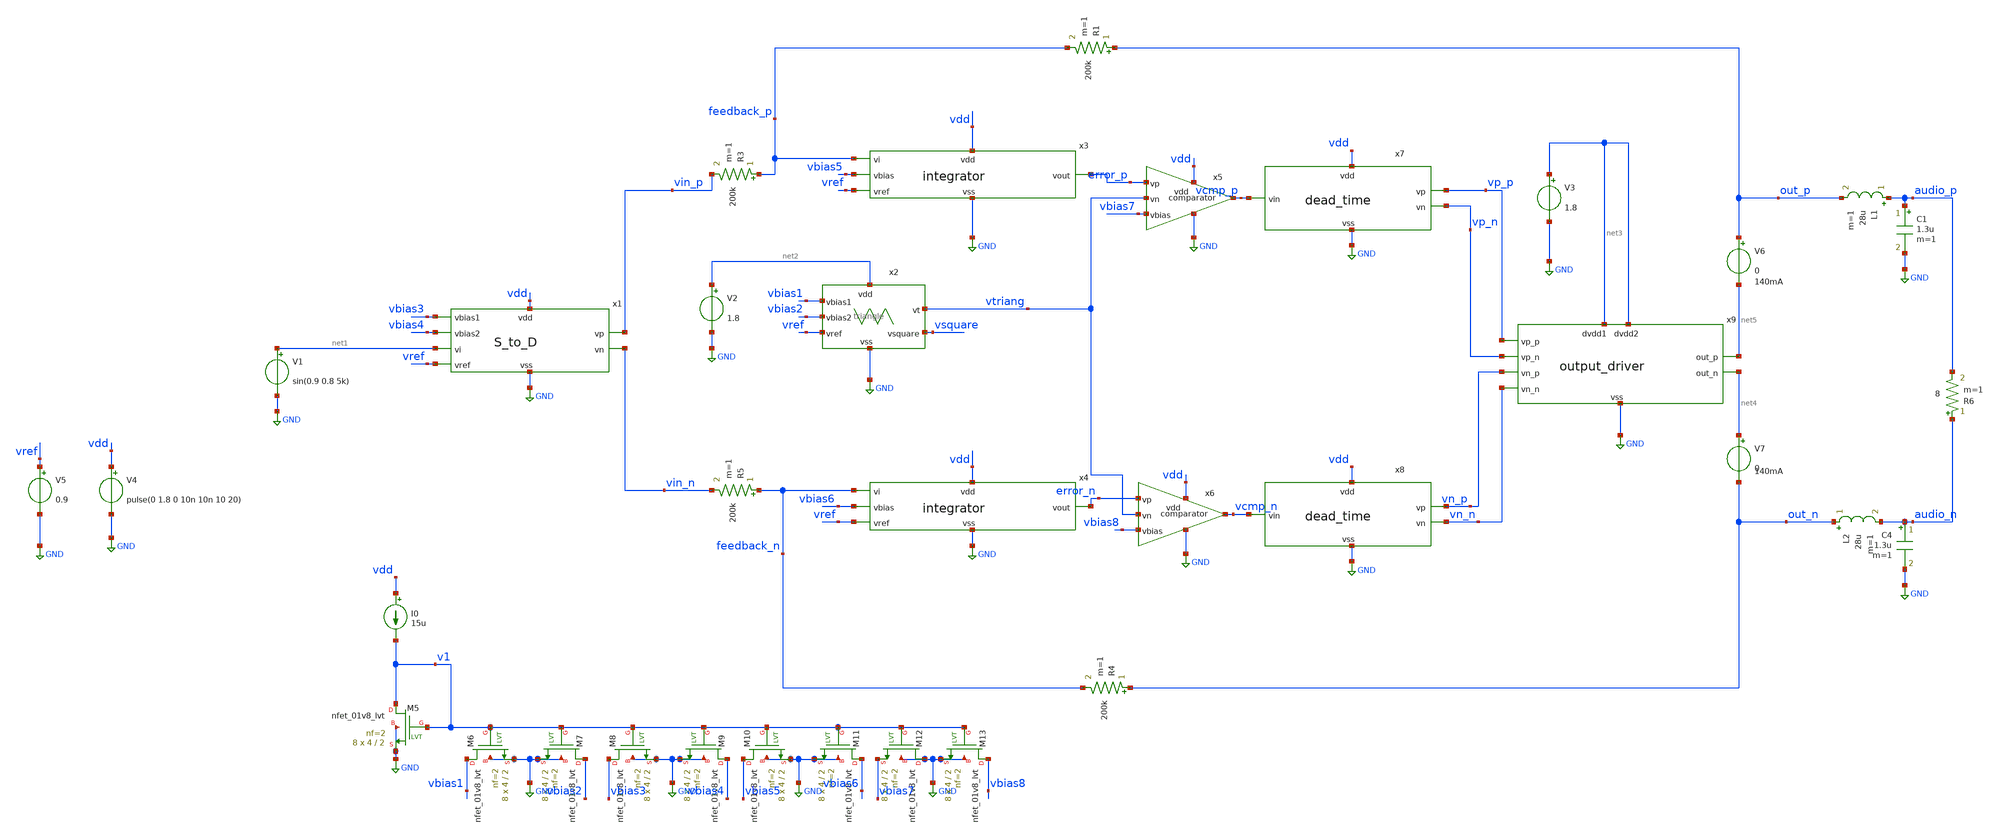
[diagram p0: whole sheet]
** sch_path: xschem/src/Class_D/Class_D_revised_tb.sch
**.subckt Class_D_revised_tb
V1 net1 GND sin(0.9 0.8 5k)
V5 vref GND 0.9
L1 audio_p out_p 28u m=1
C1 audio_p GND 1.3u m=1
R1 out_p feedback_p 200k m=1
R3 feedback_p vin_p 200k m=1
R4 out_n feedback_n 200k m=1
R5 feedback_n vin_n 200k m=1
L2 out_n audio_n 28u m=1
C4 audio_n GND 1.3u m=1
R6 audio_n audio_p 8 m=1
V4 vdd GND pulse(0 1.8 0 10n 10n 10 20)
I0 vdd v1 15u
XM5 v1 v1 GND GND sky130_fd_pr__nfet_01v8_lvt L=2 W=4 nf=2 ad='int((nf+1)/2) * W/nf * 0.29' as='int((nf+2)/2) * W/nf * 0.29'
+ pd='2*int((nf+1)/2) * (W/nf + 0.29)' ps='2*int((nf+2)/2) * (W/nf + 0.29)' nrd='0.29 / W' nrs='0.29 / W'
+ sa=0 sb=0 sd=0 mult=8 m=8
XM6 vbias1 v1 GND GND sky130_fd_pr__nfet_01v8_lvt L=2 W=4 nf=2 ad='int((nf+1)/2) * W/nf * 0.29' as='int((nf+2)/2) * W/nf * 0.29'
+ pd='2*int((nf+1)/2) * (W/nf + 0.29)' ps='2*int((nf+2)/2) * (W/nf + 0.29)' nrd='0.29 / W' nrs='0.29 / W'
+ sa=0 sb=0 sd=0 mult=8 m=8
XM7 vbias2 v1 GND GND sky130_fd_pr__nfet_01v8_lvt L=2 W=4 nf=2 ad='int((nf+1)/2) * W/nf * 0.29' as='int((nf+2)/2) * W/nf * 0.29'
+ pd='2*int((nf+1)/2) * (W/nf + 0.29)' ps='2*int((nf+2)/2) * (W/nf + 0.29)' nrd='0.29 / W' nrs='0.29 / W'
+ sa=0 sb=0 sd=0 mult=8 m=8
XM8 vbias3 v1 GND GND sky130_fd_pr__nfet_01v8_lvt L=2 W=4 nf=2 ad='int((nf+1)/2) * W/nf * 0.29' as='int((nf+2)/2) * W/nf * 0.29'
+ pd='2*int((nf+1)/2) * (W/nf + 0.29)' ps='2*int((nf+2)/2) * (W/nf + 0.29)' nrd='0.29 / W' nrs='0.29 / W'
+ sa=0 sb=0 sd=0 mult=8 m=8
XM9 vbias4 v1 GND GND sky130_fd_pr__nfet_01v8_lvt L=2 W=4 nf=2 ad='int((nf+1)/2) * W/nf * 0.29' as='int((nf+2)/2) * W/nf * 0.29'
+ pd='2*int((nf+1)/2) * (W/nf + 0.29)' ps='2*int((nf+2)/2) * (W/nf + 0.29)' nrd='0.29 / W' nrs='0.29 / W'
+ sa=0 sb=0 sd=0 mult=8 m=8
XM10 vbias5 v1 GND GND sky130_fd_pr__nfet_01v8_lvt L=2 W=4 nf=2 ad='int((nf+1)/2) * W/nf * 0.29' as='int((nf+2)/2) * W/nf * 0.29'
+ pd='2*int((nf+1)/2) * (W/nf + 0.29)' ps='2*int((nf+2)/2) * (W/nf + 0.29)' nrd='0.29 / W' nrs='0.29 / W'
+ sa=0 sb=0 sd=0 mult=8 m=8
XM11 vbias6 v1 GND GND sky130_fd_pr__nfet_01v8_lvt L=2 W=4 nf=2 ad='int((nf+1)/2) * W/nf * 0.29' as='int((nf+2)/2) * W/nf * 0.29'
+ pd='2*int((nf+1)/2) * (W/nf + 0.29)' ps='2*int((nf+2)/2) * (W/nf + 0.29)' nrd='0.29 / W' nrs='0.29 / W'
+ sa=0 sb=0 sd=0 mult=8 m=8
XM12 GND v1 vbias7 GND sky130_fd_pr__nfet_01v8_lvt L=2 W=4 nf=2 ad='int((nf+1)/2) * W/nf * 0.29' as='int((nf+2)/2) * W/nf * 0.29'
+ pd='2*int((nf+1)/2) * (W/nf + 0.29)' ps='2*int((nf+2)/2) * (W/nf + 0.29)' nrd='0.29 / W' nrs='0.29 / W'
+ sa=0 sb=0 sd=0 mult=8 m=8
XM13 vbias8 v1 GND GND sky130_fd_pr__nfet_01v8_lvt L=2 W=4 nf=2 ad='int((nf+1)/2) * W/nf * 0.29' as='int((nf+2)/2) * W/nf * 0.29'
+ pd='2*int((nf+1)/2) * (W/nf + 0.29)' ps='2*int((nf+2)/2) * (W/nf + 0.29)' nrd='0.29 / W' nrs='0.29 / W'
+ sa=0 sb=0 sd=0 mult=8 m=8
V2 net2 GND 1.8
V3 net3 GND 1.8
x1 vdd vbias3 vbias4 net1 vref GND vin_n vin_p S_to_D
x2 net2 vbias1 vbias2 vref GND vsquare vtriang triangle
x3 vdd feedback_p vbias5 vref GND error_p integrator
x4 vdd feedback_n vbias6 vref GND error_n integrator
x5 vdd error_p vtriang vbias7 GND vcmp_p comparator
x6 vdd error_n vtriang vbias8 GND vcmp_n comparator
x7 vdd vcmp_p vp_p vp_n GND dead_time
x8 vdd vcmp_n vn_p vn_n GND dead_time
x9 net3 vp_p net5 GND vp_n net3 vn_p net4 vn_n output_driver
V6 out_p net5 0
V7 net4 out_n 0
**** begin user architecture code


.option rshunt=1e20
.nodeset V(audio_p)=0.9 V(audio_n)=0.9 V(vp_p)=0.79 V(vn_p)=0 V(vcmp_p)=0.859  V(vp_n)=0.79
+ V(vn_n)=0 V(vcmp_n)=0.859 v(vin_p)=0.9 v(vin_n)=0.9 v(vtriang)=0.9
*.nodeset all=0.9
*.option VNTOL=1e-6 ABSTOL=1e-9
*.option savecurrents
*set the absolute voltage error tolerance and absolute current error tolerance
.control
save out_p out_n audio_p audio_n I(V4) I(V2) @r6[i] @r1[i] i(v3) i(v6) vtriang vin_p vin_n error_p
+ error_n vcmp_p vcmp_n vp_p vp_n vn_p vn_n i(v7)
*save vtriang audio_p audio_n I(V2) @r6[i] out_p out_n
*op
tran 3n 10m
*linearize V(audio)
*linearize V(out)
*fft V(out)
*fft V(audio)
*plot mag(V(audio))
*plot mag(V(out))
let pout=@r6[i]*(V(audio_p)-V(audio_n))
let pin=1.8*(I(V4)+I(V2)+I(V3))
meas tran pload avg pout from=2m to=9m
meas tran p_supply avg pin from=2m to=9m
*print pload/p_supply
set nfreqs=20
*fourier 10k V(out_p)-V(out_n)

fourier 5k V(audio_p)-V(audio_n)
write class_d_5k_08_output_current_test.raw

.endc





.include /home/eda/pdk/skywater-pdk/libraries/sky130_fd_pr_ngspice/latest/models/corners/tt.spice
.include /home/eda/magic/class_d_audio_amplifier/OTA/OTA_int_post.spice
.include /home/eda/magic/class_d_audio_amplifier/OTA/OTA_post.spice
.include /home/eda/magic/class_d_audio_amplifier/S_to_D/S_to_D_post.spice
.include /home/eda/magic/class_d_audio_amplifier/triang/triangle_post.spice
.include /home/eda/magic/class_d_audio_amplifier/comparator/comparator_post.spice
.include /home/eda/magic/class_d_audio_amplifier/dead_time/dead_time_post.spice
.include /home/eda/magic/class_d_audio_amplifier/output_driver/output_driver_post.spice
* Resistor$::SKYWATER_MODELS/Capacitor
.include $::SKYWATER_MODELS/models/r+c/res_typical__cap_typical.spice
.include $::SKYWATER_MODELS/models/r+c/res_typical__cap_typical__lin.spice
* Special cells
.include $::SKYWATER_MODELS/models/corners/tt/specialized_cells.spice


**** end user architecture code
**.ends

* expanding   symbol:  src/S_to_D/S_to_D.sym # of pins=8
** sym_path: xschem/src/S_to_D/S_to_D.sym
** sch_path: xschem/src/S_to_D/S_to_D.sch
.subckt S_to_D vdd vbias1 vbias2 vi vref vss vn vp
*.iopin vdd
*.iopin vss
*.ipin vi
*.opin vp
*.opin vn
*.ipin vref
*.ipin vbias1
*.ipin vbias2
x1 vdd vref v1 vbias2 vss vn OTA
XR2 vn v1 vss sky130_fd_pr__res_xhigh_po L=10 mult=1 m=1
x2 vdd vi vp vbias1 vss vp OTA
XR1 v1 vi vss sky130_fd_pr__res_xhigh_po L=10 mult=1 m=1
.ends


* expanding   symbol:  src/triangle/triangle.sym # of pins=7
** sym_path: xschem/src/triangle/triangle.sym
** sch_path: xschem/src/triangle/triangle.sch
.subckt triangle vdd vbias1 vbias2 vref vss vsquare vt
*.iopin vdd
*.ipin vbias1
*.opin vt
*.ipin vref
*.opin vsquare
*.iopin vss
*.ipin vbias2
XR3 vsquare vi vss sky130_fd_pr__res_xhigh_po L=32 mult=1 m=1
XR1 vt vcmp vss sky130_fd_pr__res_xhigh_po L=4 mult=1 m=1
XR2 vcmp vsquare vss sky130_fd_pr__res_xhigh_po L=9 mult=1 m=1
x1 vdd vref vi vbias1 vss vt OTA_tri
x2 vdd vcmp vref vbias2 vss vsquare OTA
XC1 vi vt sky130_fd_pr__cap_mim_m3_1 W=15 L=15 MF=8 m=8
.ends


* expanding   symbol:  src/integrator/integrator.sym # of pins=6
** sym_path: xschem/src/integrator/integrator.sym
** sch_path: xschem/src/integrator/integrator.sch
.subckt integrator vdd vi vbias vref vss vout
*.ipin vi
*.ipin vbias
*.iopin vss
*.iopin vdd
*.opin vout
*.ipin vref
x1 vdd vref vi vbias vss vout OTA_int
XC1 vi vout sky130_fd_pr__cap_mim_m3_1 W=17.5 L=17.5 MF=16 m=16
.ends


* expanding   symbol:  src/comparator/comparator.sym # of pins=6
** sym_path: xschem/src/comparator/comparator.sym
** sch_path: xschem/src/comparator/comparator.sch
.subckt comparator vdd vp vn vbias vss vout
*.ipin vp
*.ipin vn
*.ipin vbias
*.iopin vss
*.iopin vdd
*.opin vout
XM1 v1 vp vc vc sky130_fd_pr__pfet_01v8_lvt L=1 W=4 nf=1 ad='int((nf+1)/2) * W/nf * 0.29' as='int((nf+2)/2) * W/nf * 0.29'
+ pd='2*int((nf+1)/2) * (W/nf + 0.29)' ps='2*int((nf+2)/2) * (W/nf + 0.29)' nrd='0.29 / W' nrs='0.29 / W'
+ sa=0 sb=0 sd=0 mult=16 m=16
XM2 vf vn vc vc sky130_fd_pr__pfet_01v8_lvt L=1 W=4 nf=1 ad='int((nf+1)/2) * W/nf * 0.29' as='int((nf+2)/2) * W/nf * 0.29'
+ pd='2*int((nf+1)/2) * (W/nf + 0.29)' ps='2*int((nf+2)/2) * (W/nf + 0.29)' nrd='0.29 / W' nrs='0.29 / W'
+ sa=0 sb=0 sd=0 mult=16 m=16
XM3 vc vbias vdd vdd sky130_fd_pr__pfet_01v8_lvt L=1 W=2 nf=2 ad='int((nf+1)/2) * W/nf * 0.29' as='int((nf+2)/2) * W/nf * 0.29'
+ pd='2*int((nf+1)/2) * (W/nf + 0.29)' ps='2*int((nf+2)/2) * (W/nf + 0.29)' nrd='0.29 / W' nrs='0.29 / W'
+ sa=0 sb=0 sd=0 mult=24 m=24
XM4 v1 vf vss vss sky130_fd_pr__nfet_01v8_lvt L=1 W=1 nf=1 ad='int((nf+1)/2) * W/nf * 0.29' as='int((nf+2)/2) * W/nf * 0.29'
+ pd='2*int((nf+1)/2) * (W/nf + 0.29)' ps='2*int((nf+2)/2) * (W/nf + 0.29)' nrd='0.29 / W' nrs='0.29 / W'
+ sa=0 sb=0 sd=0 mult=16 m=16
XM5 vf vf vss vss sky130_fd_pr__nfet_01v8_lvt L=1 W=1 nf=1 ad='int((nf+1)/2) * W/nf * 0.29' as='int((nf+2)/2) * W/nf * 0.29'
+ pd='2*int((nf+1)/2) * (W/nf + 0.29)' ps='2*int((nf+2)/2) * (W/nf + 0.29)' nrd='0.29 / W' nrs='0.29 / W'
+ sa=0 sb=0 sd=0 mult=16 m=16
XM6 vbias vbias vdd vdd sky130_fd_pr__pfet_01v8_lvt L=1 W=2 nf=2 ad='int((nf+1)/2) * W/nf * 0.29' as='int((nf+2)/2) * W/nf * 0.29'
+ pd='2*int((nf+1)/2) * (W/nf + 0.29)' ps='2*int((nf+2)/2) * (W/nf + 0.29)' nrd='0.29 / W' nrs='0.29 / W'
+ sa=0 sb=0 sd=0 mult=24 m=24
XM7 vout vbias vdd vdd sky130_fd_pr__pfet_01v8_lvt L=1 W=2 nf=2 ad='int((nf+1)/2) * W/nf * 0.29' as='int((nf+2)/2) * W/nf * 0.29'
+ pd='2*int((nf+1)/2) * (W/nf + 0.29)' ps='2*int((nf+2)/2) * (W/nf + 0.29)' nrd='0.29 / W' nrs='0.29 / W'
+ sa=0 sb=0 sd=0 mult=48 m=48
XM8 vout v1 vss vss sky130_fd_pr__nfet_01v8_lvt L=1 W=1 nf=1 ad='int((nf+1)/2) * W/nf * 0.29' as='int((nf+2)/2) * W/nf * 0.29'
+ pd='2*int((nf+1)/2) * (W/nf + 0.29)' ps='2*int((nf+2)/2) * (W/nf + 0.29)' nrd='0.29 / W' nrs='0.29 / W'
+ sa=0 sb=0 sd=0 mult=64 m=64
.ends


* expanding   symbol:  src/dead_time/dead_time.sym # of pins=5
** sym_path: xschem/src/dead_time/dead_time.sym
** sch_path: xschem/src/dead_time/dead_time.sch
.subckt dead_time vdd vin vp vn vss
*.ipin vin
*.iopin vdd
*.opin vp
*.iopin vss
*.opin vn
x1 vdd vin vinn vss inverter
x2 vdd net1 vin net4 vss nand
x3 vdd net2 net3 vinn vss nand
XC1 net1 vss sky130_fd_pr__cap_mim_m3_1 W=17.75 L=17.75 MF=16 m=16
XM3 net5 net1 vss vss sky130_fd_pr__nfet_01v8 L=0.15 W=5 nf=2 ad='int((nf+1)/2) * W/nf * 0.29' as='int((nf+2)/2) * W/nf * 0.29'
+ pd='2*int((nf+1)/2) * (W/nf + 0.29)' ps='2*int((nf+2)/2) * (W/nf + 0.29)' nrd='0.29 / W' nrs='0.29 / W'
+ sa=0 sb=0 sd=0 mult=1 m=1
XM1 net5 net1 vdd vdd sky130_fd_pr__pfet_01v8 L=0.15 W=10 nf=2 ad='int((nf+1)/2) * W/nf * 0.29' as='int((nf+2)/2) * W/nf * 0.29'
+ pd='2*int((nf+1)/2) * (W/nf + 0.29)' ps='2*int((nf+2)/2) * (W/nf + 0.29)' nrd='0.29 / W' nrs='0.29 / W'
+ sa=0 sb=0 sd=0 mult=1 m=1
XM2 net3 net5 vss vss sky130_fd_pr__nfet_01v8 L=0.15 W=20 nf=8 ad='int((nf+1)/2) * W/nf * 0.29' as='int((nf+2)/2) * W/nf * 0.29'
+ pd='2*int((nf+1)/2) * (W/nf + 0.29)' ps='2*int((nf+2)/2) * (W/nf + 0.29)' nrd='0.29 / W' nrs='0.29 / W'
+ sa=0 sb=0 sd=0 mult=1 m=1
XM4 net3 net5 vdd vdd sky130_fd_pr__pfet_01v8 L=0.15 W=40 nf=8 ad='int((nf+1)/2) * W/nf * 0.29' as='int((nf+2)/2) * W/nf * 0.29'
+ pd='2*int((nf+1)/2) * (W/nf + 0.29)' ps='2*int((nf+2)/2) * (W/nf + 0.29)' nrd='0.29 / W' nrs='0.29 / W'
+ sa=0 sb=0 sd=0 mult=1 m=1
XM5 net6 net3 vss vss sky130_fd_pr__nfet_01v8 L=0.15 W=90 nf=36 ad='int((nf+1)/2) * W/nf * 0.29' as='int((nf+2)/2) * W/nf * 0.29'
+ pd='2*int((nf+1)/2) * (W/nf + 0.29)' ps='2*int((nf+2)/2) * (W/nf + 0.29)' nrd='0.29 / W' nrs='0.29 / W'
+ sa=0 sb=0 sd=0 mult=1 m=1
XM6 net6 net3 vdd vdd sky130_fd_pr__pfet_01v8 L=0.15 W=180 nf=36 ad='int((nf+1)/2) * W/nf * 0.29' as='int((nf+2)/2) * W/nf * 0.29'
+ pd='2*int((nf+1)/2) * (W/nf + 0.29)' ps='2*int((nf+2)/2) * (W/nf + 0.29)' nrd='0.29 / W' nrs='0.29 / W'
+ sa=0 sb=0 sd=0 mult=1 m=1
XM7 vp net6 vss vss sky130_fd_pr__nfet_01v8 L=0.15 W=200 nf=81 ad='int((nf+1)/2) * W/nf * 0.29' as='int((nf+2)/2) * W/nf * 0.29'
+ pd='2*int((nf+1)/2) * (W/nf + 0.29)' ps='2*int((nf+2)/2) * (W/nf + 0.29)' nrd='0.29 / W' nrs='0.29 / W'
+ sa=0 sb=0 sd=0 mult=2 m=2
XM8 vp net6 vdd vdd sky130_fd_pr__pfet_01v8 L=0.15 W=400 nf=81 ad='int((nf+1)/2) * W/nf * 0.29' as='int((nf+2)/2) * W/nf * 0.29'
+ pd='2*int((nf+1)/2) * (W/nf + 0.29)' ps='2*int((nf+2)/2) * (W/nf + 0.29)' nrd='0.29 / W' nrs='0.29 / W'
+ sa=0 sb=0 sd=0 mult=2 m=2
XM9 net7 net2 vss vss sky130_fd_pr__nfet_01v8 L=0.15 W=5 nf=2 ad='int((nf+1)/2) * W/nf * 0.29' as='int((nf+2)/2) * W/nf * 0.29'
+ pd='2*int((nf+1)/2) * (W/nf + 0.29)' ps='2*int((nf+2)/2) * (W/nf + 0.29)' nrd='0.29 / W' nrs='0.29 / W'
+ sa=0 sb=0 sd=0 mult=1 m=1
XM10 net7 net2 vdd vdd sky130_fd_pr__pfet_01v8 L=0.15 W=10 nf=2 ad='int((nf+1)/2) * W/nf * 0.29' as='int((nf+2)/2) * W/nf * 0.29'
+ pd='2*int((nf+1)/2) * (W/nf + 0.29)' ps='2*int((nf+2)/2) * (W/nf + 0.29)' nrd='0.29 / W' nrs='0.29 / W'
+ sa=0 sb=0 sd=0 mult=1 m=1
XM11 net4 net7 vss vss sky130_fd_pr__nfet_01v8 L=0.15 W=20 nf=8 ad='int((nf+1)/2) * W/nf * 0.29' as='int((nf+2)/2) * W/nf * 0.29'
+ pd='2*int((nf+1)/2) * (W/nf + 0.29)' ps='2*int((nf+2)/2) * (W/nf + 0.29)' nrd='0.29 / W' nrs='0.29 / W'
+ sa=0 sb=0 sd=0 mult=1 m=1
XM12 net4 net7 vdd vdd sky130_fd_pr__pfet_01v8 L=0.15 W=40 nf=8 ad='int((nf+1)/2) * W/nf * 0.29' as='int((nf+2)/2) * W/nf * 0.29'
+ pd='2*int((nf+1)/2) * (W/nf + 0.29)' ps='2*int((nf+2)/2) * (W/nf + 0.29)' nrd='0.29 / W' nrs='0.29 / W'
+ sa=0 sb=0 sd=0 mult=1 m=1
XM13 vn net4 vss vss sky130_fd_pr__nfet_01v8 L=0.15 W=90 nf=36 ad='int((nf+1)/2) * W/nf * 0.29' as='int((nf+2)/2) * W/nf * 0.29'
+ pd='2*int((nf+1)/2) * (W/nf + 0.29)' ps='2*int((nf+2)/2) * (W/nf + 0.29)' nrd='0.29 / W' nrs='0.29 / W'
+ sa=0 sb=0 sd=0 mult=1 m=1
XM14 vn net4 vdd vdd sky130_fd_pr__pfet_01v8 L=0.15 W=180 nf=36 ad='int((nf+1)/2) * W/nf * 0.29' as='int((nf+2)/2) * W/nf * 0.29'
+ pd='2*int((nf+1)/2) * (W/nf + 0.29)' ps='2*int((nf+2)/2) * (W/nf + 0.29)' nrd='0.29 / W' nrs='0.29 / W'
+ sa=0 sb=0 sd=0 mult=1 m=1
XC2 net2 vss sky130_fd_pr__cap_mim_m3_1 W=17.75 L=17.75 MF=16 m=16
.ends


* expanding   symbol:  src/output_driver/output_driver.sym # of pins=9
** sym_path: xschem/src/output_driver/output_driver.sym
** sch_path: xschem/src/output_driver/output_driver.sch
.subckt output_driver dvdd1 vp_p out_p vss vp_n dvdd2 vn_p out_n vn_n
*.ipin vp_p
*.ipin vp_n
*.ipin vn_p
*.ipin vn_n
*.opin out_p
*.opin out_n
*.iopin dvdd1
*.iopin vss
*.iopin dvdd2
x1 dvdd1 vss vp_p out_p vp_n half_driver
x2 dvdd2 vss vn_p out_n vn_n half_driver
.ends


* expanding   symbol:  src/OTA/OTA.sym # of pins=6
** sym_path: xschem/src/OTA/OTA.sym
** sch_path: xschem/src/OTA/OTA.sch
.subckt OTA vdd vp vn vbias vss vout
*.ipin vp
*.ipin vn
*.ipin vbias
*.iopin vss
*.iopin vdd
*.opin vout
XM1 v1 vp vc vc sky130_fd_pr__pfet_01v8_lvt L=1 W=4 nf=1 ad='int((nf+1)/2) * W/nf * 0.29' as='int((nf+2)/2) * W/nf * 0.29'
+ pd='2*int((nf+1)/2) * (W/nf + 0.29)' ps='2*int((nf+2)/2) * (W/nf + 0.29)' nrd='0.29 / W' nrs='0.29 / W'
+ sa=0 sb=0 sd=0 mult=16 m=16
XM2 vf vn vc vc sky130_fd_pr__pfet_01v8_lvt L=1 W=4 nf=1 ad='int((nf+1)/2) * W/nf * 0.29' as='int((nf+2)/2) * W/nf * 0.29'
+ pd='2*int((nf+1)/2) * (W/nf + 0.29)' ps='2*int((nf+2)/2) * (W/nf + 0.29)' nrd='0.29 / W' nrs='0.29 / W'
+ sa=0 sb=0 sd=0 mult=16 m=16
XM3 vc vbias vdd vdd sky130_fd_pr__pfet_01v8_lvt L=1 W=2 nf=2 ad='int((nf+1)/2) * W/nf * 0.29' as='int((nf+2)/2) * W/nf * 0.29'
+ pd='2*int((nf+1)/2) * (W/nf + 0.29)' ps='2*int((nf+2)/2) * (W/nf + 0.29)' nrd='0.29 / W' nrs='0.29 / W'
+ sa=0 sb=0 sd=0 mult=24 m=24
XM4 v1 vf vss vss sky130_fd_pr__nfet_01v8_lvt L=1 W=1 nf=1 ad='int((nf+1)/2) * W/nf * 0.29' as='int((nf+2)/2) * W/nf * 0.29'
+ pd='2*int((nf+1)/2) * (W/nf + 0.29)' ps='2*int((nf+2)/2) * (W/nf + 0.29)' nrd='0.29 / W' nrs='0.29 / W'
+ sa=0 sb=0 sd=0 mult=16 m=16
XM5 vf vf vss vss sky130_fd_pr__nfet_01v8_lvt L=1 W=1 nf=1 ad='int((nf+1)/2) * W/nf * 0.29' as='int((nf+2)/2) * W/nf * 0.29'
+ pd='2*int((nf+1)/2) * (W/nf + 0.29)' ps='2*int((nf+2)/2) * (W/nf + 0.29)' nrd='0.29 / W' nrs='0.29 / W'
+ sa=0 sb=0 sd=0 mult=16 m=16
XM6 vbias vbias vdd vdd sky130_fd_pr__pfet_01v8_lvt L=1 W=2 nf=2 ad='int((nf+1)/2) * W/nf * 0.29' as='int((nf+2)/2) * W/nf * 0.29'
+ pd='2*int((nf+1)/2) * (W/nf + 0.29)' ps='2*int((nf+2)/2) * (W/nf + 0.29)' nrd='0.29 / W' nrs='0.29 / W'
+ sa=0 sb=0 sd=0 mult=24 m=24
XM7 vout vbias vdd vdd sky130_fd_pr__pfet_01v8_lvt L=1 W=2 nf=2 ad='int((nf+1)/2) * W/nf * 0.29' as='int((nf+2)/2) * W/nf * 0.29'
+ pd='2*int((nf+1)/2) * (W/nf + 0.29)' ps='2*int((nf+2)/2) * (W/nf + 0.29)' nrd='0.29 / W' nrs='0.29 / W'
+ sa=0 sb=0 sd=0 mult=48 m=48
XM8 vout v1 vss vss sky130_fd_pr__nfet_01v8_lvt L=1 W=1 nf=1 ad='int((nf+1)/2) * W/nf * 0.29' as='int((nf+2)/2) * W/nf * 0.29'
+ pd='2*int((nf+1)/2) * (W/nf + 0.29)' ps='2*int((nf+2)/2) * (W/nf + 0.29)' nrd='0.29 / W' nrs='0.29 / W'
+ sa=0 sb=0 sd=0 mult=64 m=64
XR1 v1 net1 vss sky130_fd_pr__res_xhigh_po W=0.35 L=0.5 mult=1 m=1
XC2 net1 vout sky130_fd_pr__cap_mim_m3_1 W=14 L=14 MF=1 m=1
.ends


* expanding   symbol:  src/OTA_tri/OTA_tri.sym # of pins=6
** sym_path: xschem/src/OTA_tri/OTA_tri.sym
** sch_path: xschem/src/OTA_tri/OTA_tri.sch
.subckt OTA_tri vdd vp vn vbias vss vout
*.ipin vp
*.ipin vn
*.ipin vbias
*.iopin vss
*.iopin vdd
*.opin vout
XM1 v1 vp vc vc sky130_fd_pr__pfet_01v8_lvt L=1 W=4 nf=1 ad='int((nf+1)/2) * W/nf * 0.29' as='int((nf+2)/2) * W/nf * 0.29'
+ pd='2*int((nf+1)/2) * (W/nf + 0.29)' ps='2*int((nf+2)/2) * (W/nf + 0.29)' nrd='0.29 / W' nrs='0.29 / W'
+ sa=0 sb=0 sd=0 mult=16 m=16
XM2 vf vn vc vc sky130_fd_pr__pfet_01v8_lvt L=1 W=4 nf=1 ad='int((nf+1)/2) * W/nf * 0.29' as='int((nf+2)/2) * W/nf * 0.29'
+ pd='2*int((nf+1)/2) * (W/nf + 0.29)' ps='2*int((nf+2)/2) * (W/nf + 0.29)' nrd='0.29 / W' nrs='0.29 / W'
+ sa=0 sb=0 sd=0 mult=16 m=16
XM3 vc vbias vdd vdd sky130_fd_pr__pfet_01v8_lvt L=1 W=2 nf=2 ad='int((nf+1)/2) * W/nf * 0.29' as='int((nf+2)/2) * W/nf * 0.29'
+ pd='2*int((nf+1)/2) * (W/nf + 0.29)' ps='2*int((nf+2)/2) * (W/nf + 0.29)' nrd='0.29 / W' nrs='0.29 / W'
+ sa=0 sb=0 sd=0 mult=24 m=24
XM4 v1 vf vss vss sky130_fd_pr__nfet_01v8_lvt L=1 W=1 nf=1 ad='int((nf+1)/2) * W/nf * 0.29' as='int((nf+2)/2) * W/nf * 0.29'
+ pd='2*int((nf+1)/2) * (W/nf + 0.29)' ps='2*int((nf+2)/2) * (W/nf + 0.29)' nrd='0.29 / W' nrs='0.29 / W'
+ sa=0 sb=0 sd=0 mult=16 m=16
XM5 vf vf vss vss sky130_fd_pr__nfet_01v8_lvt L=1 W=1 nf=1 ad='int((nf+1)/2) * W/nf * 0.29' as='int((nf+2)/2) * W/nf * 0.29'
+ pd='2*int((nf+1)/2) * (W/nf + 0.29)' ps='2*int((nf+2)/2) * (W/nf + 0.29)' nrd='0.29 / W' nrs='0.29 / W'
+ sa=0 sb=0 sd=0 mult=16 m=16
XM6 vbias vbias vdd vdd sky130_fd_pr__pfet_01v8_lvt L=1 W=2 nf=2 ad='int((nf+1)/2) * W/nf * 0.29' as='int((nf+2)/2) * W/nf * 0.29'
+ pd='2*int((nf+1)/2) * (W/nf + 0.29)' ps='2*int((nf+2)/2) * (W/nf + 0.29)' nrd='0.29 / W' nrs='0.29 / W'
+ sa=0 sb=0 sd=0 mult=24 m=24
XM7 vout vbias vdd vdd sky130_fd_pr__pfet_01v8_lvt L=1 W=2 nf=3 ad='int((nf+1)/2) * W/nf * 0.29' as='int((nf+2)/2) * W/nf * 0.29'
+ pd='2*int((nf+1)/2) * (W/nf + 0.29)' ps='2*int((nf+2)/2) * (W/nf + 0.29)' nrd='0.29 / W' nrs='0.29 / W'
+ sa=0 sb=0 sd=0 mult=48 m=48
XM8 vout v1 vss vss sky130_fd_pr__nfet_01v8_lvt L=1 W=1 nf=1 ad='int((nf+1)/2) * W/nf * 0.29' as='int((nf+2)/2) * W/nf * 0.29'
+ pd='2*int((nf+1)/2) * (W/nf + 0.29)' ps='2*int((nf+2)/2) * (W/nf + 0.29)' nrd='0.29 / W' nrs='0.29 / W'
+ sa=0 sb=0 sd=0 mult=64 m=64
XC1 net1 vout sky130_fd_pr__cap_mim_m3_1 W=27 L=18 MF=1 m=1
XR1 v1 net1 vss sky130_fd_pr__res_xhigh_po W=0.35 L=1.4 mult=1 m=1
.ends


* expanding   symbol:  src/OTA_int/OTA_int.sym # of pins=6
** sym_path: xschem/src/OTA_int/OTA_int.sym
** sch_path: xschem/src/OTA_int/OTA_int.sch
.subckt OTA_int vdd vp vn vbias vss vout
*.ipin vp
*.ipin vn
*.ipin vbias
*.iopin vss
*.iopin vdd
*.opin vout
XM1 v1 vp vc vc sky130_fd_pr__pfet_01v8_lvt L=1 W=4 nf=1 ad='int((nf+1)/2) * W/nf * 0.29' as='int((nf+2)/2) * W/nf * 0.29'
+ pd='2*int((nf+1)/2) * (W/nf + 0.29)' ps='2*int((nf+2)/2) * (W/nf + 0.29)' nrd='0.29 / W' nrs='0.29 / W'
+ sa=0 sb=0 sd=0 mult=16 m=16
XM2 vf vn vc vc sky130_fd_pr__pfet_01v8_lvt L=1 W=4 nf=1 ad='int((nf+1)/2) * W/nf * 0.29' as='int((nf+2)/2) * W/nf * 0.29'
+ pd='2*int((nf+1)/2) * (W/nf + 0.29)' ps='2*int((nf+2)/2) * (W/nf + 0.29)' nrd='0.29 / W' nrs='0.29 / W'
+ sa=0 sb=0 sd=0 mult=16 m=16
XM3 vc vbias vdd vdd sky130_fd_pr__pfet_01v8_lvt L=1 W=2 nf=2 ad='int((nf+1)/2) * W/nf * 0.29' as='int((nf+2)/2) * W/nf * 0.29'
+ pd='2*int((nf+1)/2) * (W/nf + 0.29)' ps='2*int((nf+2)/2) * (W/nf + 0.29)' nrd='0.29 / W' nrs='0.29 / W'
+ sa=0 sb=0 sd=0 mult=24 m=24
XM4 v1 vf vss vss sky130_fd_pr__nfet_01v8_lvt L=1 W=1 nf=1 ad='int((nf+1)/2) * W/nf * 0.29' as='int((nf+2)/2) * W/nf * 0.29'
+ pd='2*int((nf+1)/2) * (W/nf + 0.29)' ps='2*int((nf+2)/2) * (W/nf + 0.29)' nrd='0.29 / W' nrs='0.29 / W'
+ sa=0 sb=0 sd=0 mult=16 m=16
XM5 vf vf vss vss sky130_fd_pr__nfet_01v8_lvt L=1 W=1 nf=1 ad='int((nf+1)/2) * W/nf * 0.29' as='int((nf+2)/2) * W/nf * 0.29'
+ pd='2*int((nf+1)/2) * (W/nf + 0.29)' ps='2*int((nf+2)/2) * (W/nf + 0.29)' nrd='0.29 / W' nrs='0.29 / W'
+ sa=0 sb=0 sd=0 mult=16 m=16
XM6 vbias vbias vdd vdd sky130_fd_pr__pfet_01v8_lvt L=1 W=2 nf=2 ad='int((nf+1)/2) * W/nf * 0.29' as='int((nf+2)/2) * W/nf * 0.29'
+ pd='2*int((nf+1)/2) * (W/nf + 0.29)' ps='2*int((nf+2)/2) * (W/nf + 0.29)' nrd='0.29 / W' nrs='0.29 / W'
+ sa=0 sb=0 sd=0 mult=24 m=24
XM7 vout vbias vdd vdd sky130_fd_pr__pfet_01v8_lvt L=1 W=2 nf=2 ad='int((nf+1)/2) * W/nf * 0.29' as='int((nf+2)/2) * W/nf * 0.29'
+ pd='2*int((nf+1)/2) * (W/nf + 0.29)' ps='2*int((nf+2)/2) * (W/nf + 0.29)' nrd='0.29 / W' nrs='0.29 / W'
+ sa=0 sb=0 sd=0 mult=48 m=48
XM8 vout v1 vss vss sky130_fd_pr__nfet_01v8_lvt L=1 W=1 nf=1 ad='int((nf+1)/2) * W/nf * 0.29' as='int((nf+2)/2) * W/nf * 0.29'
+ pd='2*int((nf+1)/2) * (W/nf + 0.29)' ps='2*int((nf+2)/2) * (W/nf + 0.29)' nrd='0.29 / W' nrs='0.29 / W'
+ sa=0 sb=0 sd=0 mult=64 m=64
XC1 v2 vout sky130_fd_pr__cap_mim_m3_1 W=14 L=30 MF=1 m=1
XR1 v1 v2 vss sky130_fd_pr__res_xhigh_po L=2.8 mult=1 m=1
XC2 v2 vout sky130_fd_pr__cap_mim_m3_1 W=30 L=14 MF=1 m=1
.ends


* expanding   symbol:  src/inverter/inverter.sym # of pins=4
** sym_path: xschem/src/inverter/inverter.sym
** sch_path: xschem/src/inverter/inverter.sch
.subckt inverter vdd A B vss
*.iopin vdd
*.iopin vss
*.ipin A
*.opin B
XM3 B A vss vss sky130_fd_pr__nfet_01v8 L=0.15 W=1 nf=1 ad='int((nf+1)/2) * W/nf * 0.29' as='int((nf+2)/2) * W/nf * 0.29'
+ pd='2*int((nf+1)/2) * (W/nf + 0.29)' ps='2*int((nf+2)/2) * (W/nf + 0.29)' nrd='0.29 / W' nrs='0.29 / W'
+ sa=0 sb=0 sd=0 mult=1 m=1
XM1 B A vdd vdd sky130_fd_pr__pfet_01v8 L=0.15 W=2 nf=1 ad='int((nf+1)/2) * W/nf * 0.29' as='int((nf+2)/2) * W/nf * 0.29'
+ pd='2*int((nf+1)/2) * (W/nf + 0.29)' ps='2*int((nf+2)/2) * (W/nf + 0.29)' nrd='0.29 / W' nrs='0.29 / W'
+ sa=0 sb=0 sd=0 mult=1 m=1
.ends


* expanding   symbol:  src/nand/nand.sym # of pins=5
** sym_path: xschem/src/nand/nand.sym
** sch_path: xschem/src/nand/nand.sch
.subckt nand vdd out A B vss
*.ipin A
*.ipin B
*.opin out
*.iopin vdd
*.iopin vss
XM1 out A net1 vss sky130_fd_pr__nfet_01v8 L=0.15 W=2 nf=1 ad='int((nf+1)/2) * W/nf * 0.29' as='int((nf+2)/2) * W/nf * 0.29'
+ pd='2*int((nf+1)/2) * (W/nf + 0.29)' ps='2*int((nf+2)/2) * (W/nf + 0.29)' nrd='0.29 / W' nrs='0.29 / W'
+ sa=0 sb=0 sd=0 mult=1 m=1
XM2 out A vdd vdd sky130_fd_pr__pfet_01v8 L=0.15 W=2 nf=1 ad='int((nf+1)/2) * W/nf * 0.29' as='int((nf+2)/2) * W/nf * 0.29'
+ pd='2*int((nf+1)/2) * (W/nf + 0.29)' ps='2*int((nf+2)/2) * (W/nf + 0.29)' nrd='0.29 / W' nrs='0.29 / W'
+ sa=0 sb=0 sd=0 mult=1 m=1
XM3 net1 B vss vss sky130_fd_pr__nfet_01v8 L=0.15 W=2 nf=1 ad='int((nf+1)/2) * W/nf * 0.29' as='int((nf+2)/2) * W/nf * 0.29'
+ pd='2*int((nf+1)/2) * (W/nf + 0.29)' ps='2*int((nf+2)/2) * (W/nf + 0.29)' nrd='0.29 / W' nrs='0.29 / W'
+ sa=0 sb=0 sd=0 mult=1 m=1
XM4 out B vdd vdd sky130_fd_pr__pfet_01v8 L=0.15 W=2 nf=1 ad='int((nf+1)/2) * W/nf * 0.29' as='int((nf+2)/2) * W/nf * 0.29'
+ pd='2*int((nf+1)/2) * (W/nf + 0.29)' ps='2*int((nf+2)/2) * (W/nf + 0.29)' nrd='0.29 / W' nrs='0.29 / W'
+ sa=0 sb=0 sd=0 mult=1 m=1
.ends


* expanding   symbol:  src/output_driver/half_driver.sym # of pins=5
** sym_path: xschem/src/output_driver/half_driver.sym
** sch_path: xschem/src/output_driver/half_driver.sch
.subckt half_driver vdd vss vp_p out_p vp_n
*.ipin vp_p
*.ipin vp_n
*.opin out_p
*.iopin vdd
*.iopin vss
XM1 out_p vp_p vdd vdd sky130_fd_pr__pfet_01v8 L=0.15 W=12000 nf=200 ad='int((nf+1)/2) * W/nf * 0.29'
+ as='int((nf+2)/2) * W/nf * 0.29' pd='2*int((nf+1)/2) * (W/nf + 0.29)' ps='2*int((nf+2)/2) * (W/nf + 0.29)'
+ nrd='0.29 / W' nrs='0.29 / W' sa=0 sb=0 sd=0 mult=1 m=1
XM2 out_p vp_n vss vss sky130_fd_pr__nfet_01v8 L=0.15 W=2400 nf=100 ad='int((nf+1)/2) * W/nf * 0.29'
+ as='int((nf+2)/2) * W/nf * 0.29' pd='2*int((nf+1)/2) * (W/nf + 0.29)' ps='2*int((nf+2)/2) * (W/nf + 0.29)'
+ nrd='0.29 / W' nrs='0.29 / W' sa=0 sb=0 sd=0 mult=1 m=1
.ends

.GLOBAL GND
.end
